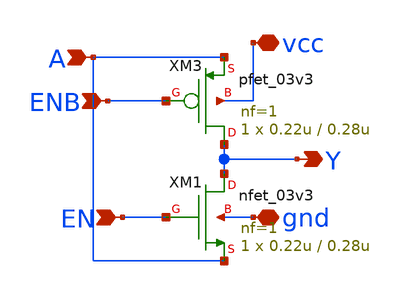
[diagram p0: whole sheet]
** sch_path: designs/schematics/mux2x1/tg.sch
**.subckt tg A EN Y ENB gnd vcc
*.ipin A
*.ipin EN
*.opin Y
*.ipin ENB
*.iopin gnd
*.iopin vcc
XM1 Y EN A gnd nfet_03v3 L=0.28u W=0.22u nf=1 ad='int((nf+1)/2) * W/nf * 0.18u' as='int((nf+2)/2) * W/nf * 0.18u'
+ pd='2*int((nf+1)/2) * (W/nf + 0.18u)' ps='2*int((nf+2)/2) * (W/nf + 0.18u)' nrd='0.18u / W' nrs='0.18u / W'
+ sa=0 sb=0 sd=0 m=1
XM3 Y ENB A vcc pfet_03v3 L=0.28u W=0.22u nf=1 ad='int((nf+1)/2) * W/nf * 0.18u' as='int((nf+2)/2) * W/nf * 0.18u'
+ pd='2*int((nf+1)/2) * (W/nf + 0.18u)' ps='2*int((nf+2)/2) * (W/nf + 0.18u)' nrd='0.18u / W' nrs='0.18u / W'
+ sa=0 sb=0 sd=0 m=1
**.ends
.end
